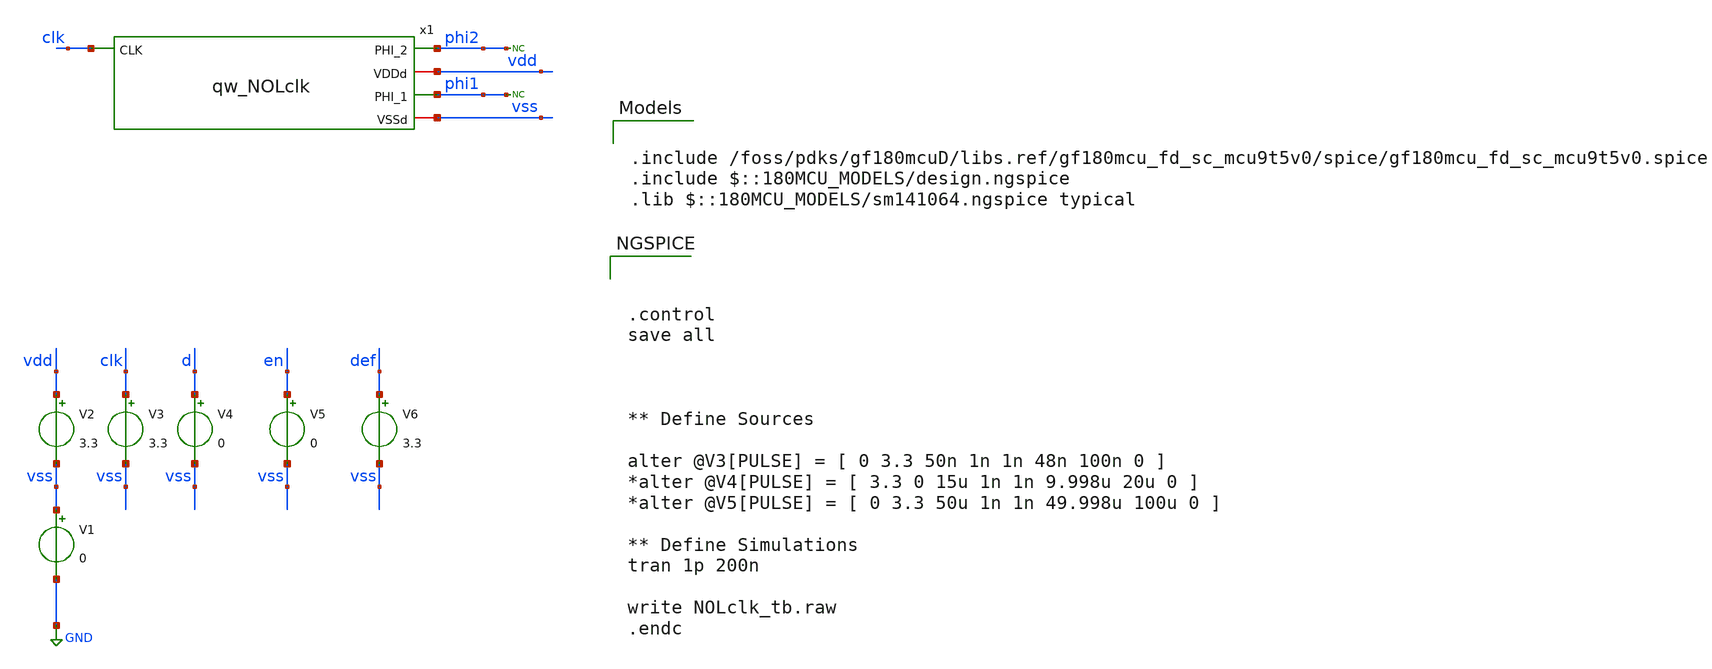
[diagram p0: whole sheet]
** sch_path: designs/libs/tb_analog/tb_qw_NOLclk/tb_qw_NOLclk.sch
**.subckt tb_qw_NOLclk
V1 vss GND 0
V2 vdd vss 3.3
V3 clk vss 3.3
V4 d vss 0
* noconn phi1
V5 en vss 0
V6 def vss 3.3
* noconn phi2
x1 phi2 clk vdd phi1 vss qw_NOLclk
**** begin user architecture code

.include /foss/pdks/gf180mcuD/libs.ref/gf180mcu_fd_sc_mcu9t5v0/spice/gf180mcu_fd_sc_mcu9t5v0.spice
.include $::180MCU_MODELS/design.ngspice
.lib $::180MCU_MODELS/sm141064.ngspice typical




.control
save all



** Define Sources

alter @V3[PULSE] = [ 0 3.3 50n 1n 1n 48n 100n 0 ]
*alter @V4[PULSE] = [ 3.3 0 15u 1n 1n 9.998u 20u 0 ]
*alter @V5[PULSE] = [ 0 3.3 50u 1n 1n 49.998u 100u 0 ]

** Define Simulations
tran 1p 200n

write NOLclk_tb.raw
.endc


**** end user architecture code
**.ends
.GLOBAL GND
.end
